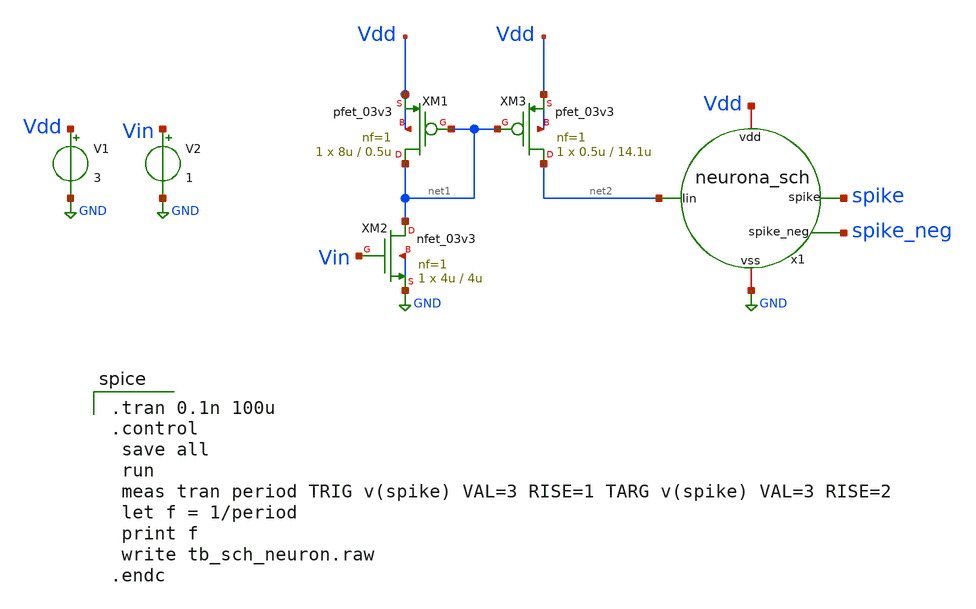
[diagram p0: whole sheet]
** sch_path: designs/libs/snn_analog/lif/sch/lif/tb_sch_neuron.sch
**.subckt tb_sch_neuron
XM1 net1 net1 Vdd Vdd pfet_03v3 L=0.5u W=8u nf=1 ad='int((nf+1)/2) * W/nf * 0.18u' as='int((nf+2)/2) * W/nf * 0.18u'
+ pd='2*int((nf+1)/2) * (W/nf + 0.18u)' ps='2*int((nf+2)/2) * (W/nf + 0.18u)' nrd='0.18u / W' nrs='0.18u / W'
+ sa=0 sb=0 sd=0 m=1
XM2 net1 Vin GND GND nfet_03v3 L=4u W=4u nf=1 ad='int((nf+1)/2) * W/nf * 0.18u' as='int((nf+2)/2) * W/nf * 0.18u'
+ pd='2*int((nf+1)/2) * (W/nf + 0.18u)' ps='2*int((nf+2)/2) * (W/nf + 0.18u)' nrd='0.18u / W' nrs='0.18u / W'
+ sa=0 sb=0 sd=0 m=1
XM3 net2 net1 Vdd Vdd pfet_03v3 L=14.1u W=0.5u nf=1 ad='int((nf+1)/2) * W/nf * 0.18u' as='int((nf+2)/2) * W/nf * 0.18u'
+ pd='2*int((nf+1)/2) * (W/nf + 0.18u)' ps='2*int((nf+2)/2) * (W/nf + 0.18u)' nrd='0.18u / W' nrs='0.18u / W'
+ sa=0 sb=0 sd=0 m=1
V1 Vdd GND 3
V2 Vin GND 1
x1 net2 Vdd GND spike spike_neg neurona_sch
**** begin user architecture code

.tran 0.1n 100u
.control
 save all
 run
 meas tran period TRIG v(spike) VAL=3 RISE=1 TARG v(spike) VAL=3 RISE=2
 let f = 1/period
 print f
 write tb_sch_neuron.raw
.endc


.include $::180MCU_MODELS/design.ngspice
.lib $::180MCU_MODELS/sm141064.ngspice typical
.lib $::180MCU_MODELS/sm141064.ngspice cap_mim
.lib $::180MCU_MODELS/sm141064.ngspice res_typical
.lib $::180MCU_MODELS/sm141064.ngspice moscap_typical
.lib $::180MCU_MODELS/sm141064.ngspice mimcap_typical
* .lib $::180MCU_MODELS/sm141064.ngspice res_statistical

**** end user architecture code
**.ends
.GLOBAL GND
.end
